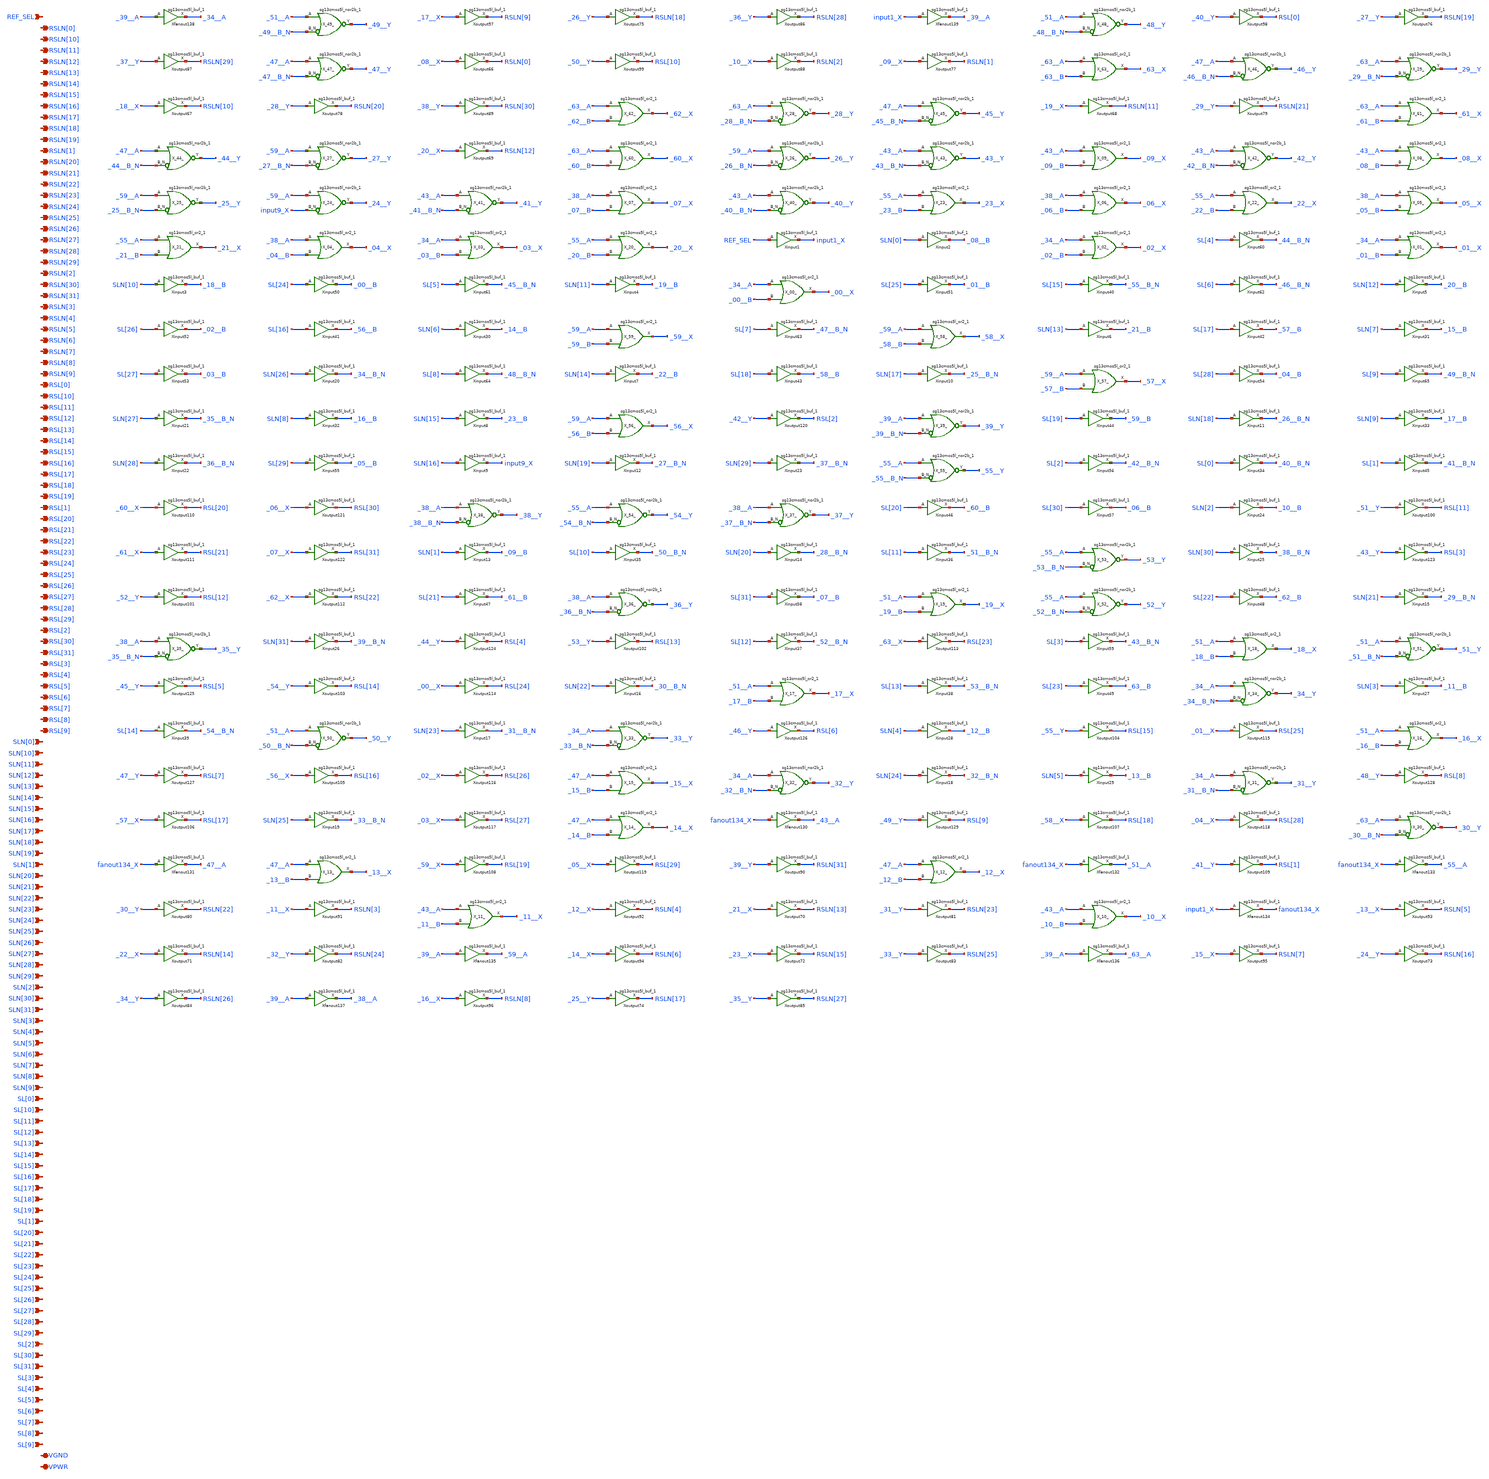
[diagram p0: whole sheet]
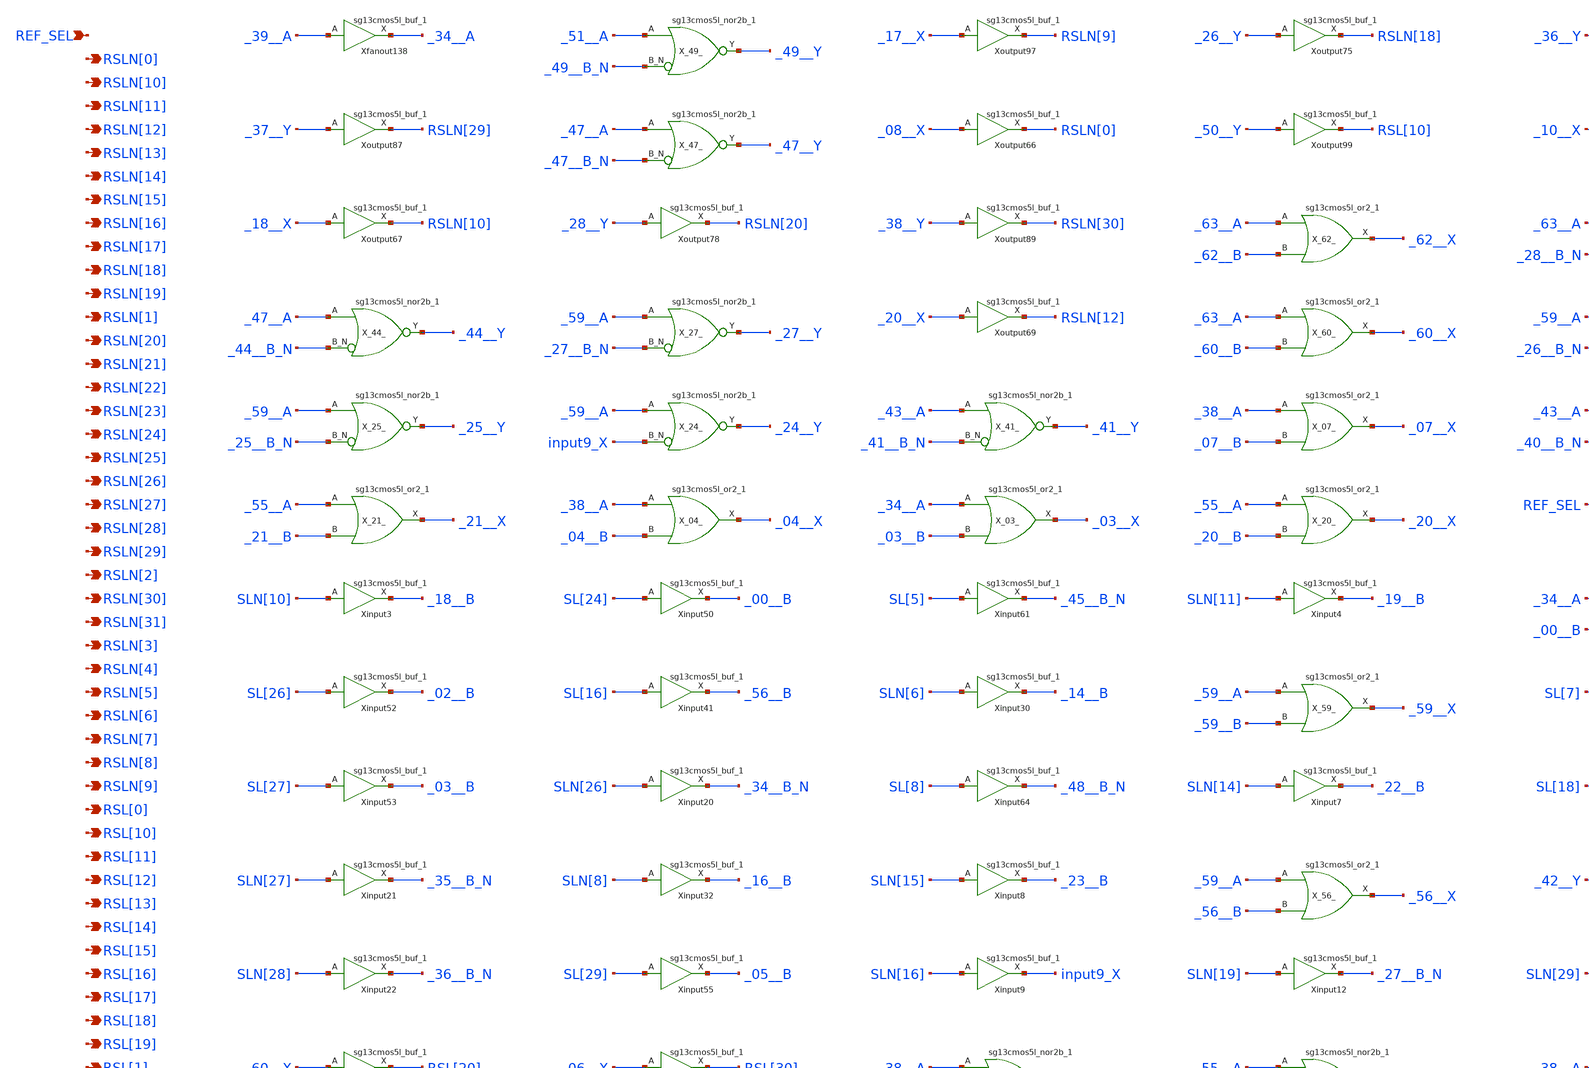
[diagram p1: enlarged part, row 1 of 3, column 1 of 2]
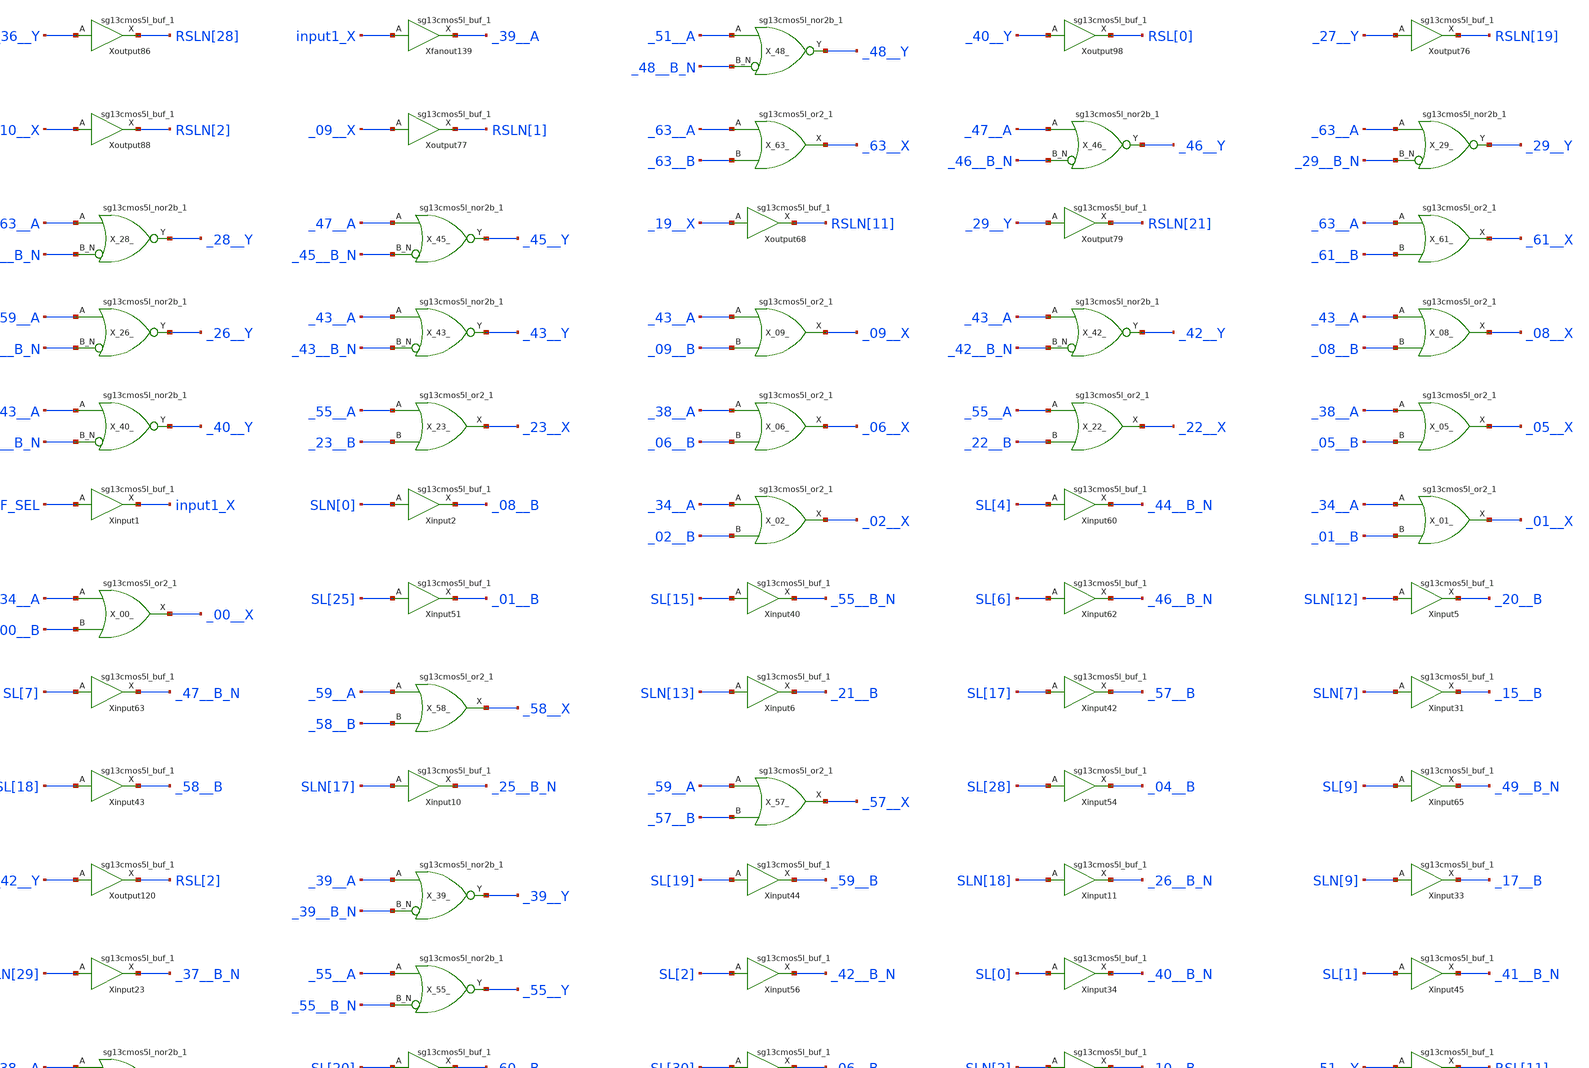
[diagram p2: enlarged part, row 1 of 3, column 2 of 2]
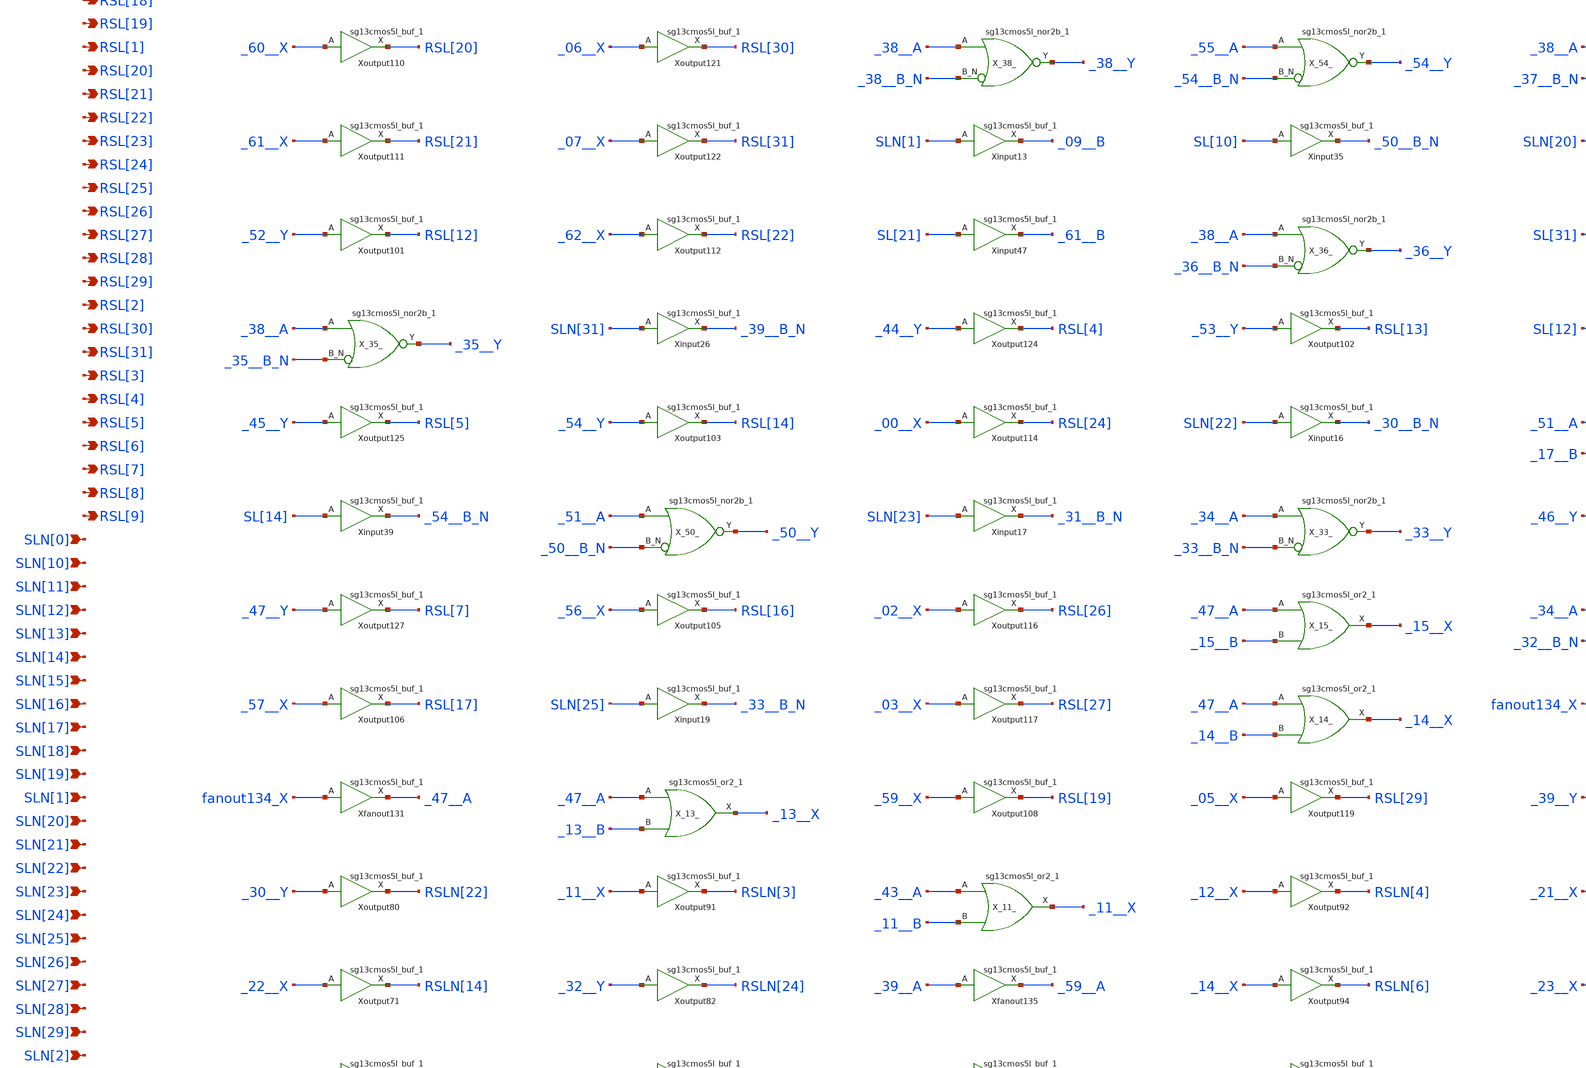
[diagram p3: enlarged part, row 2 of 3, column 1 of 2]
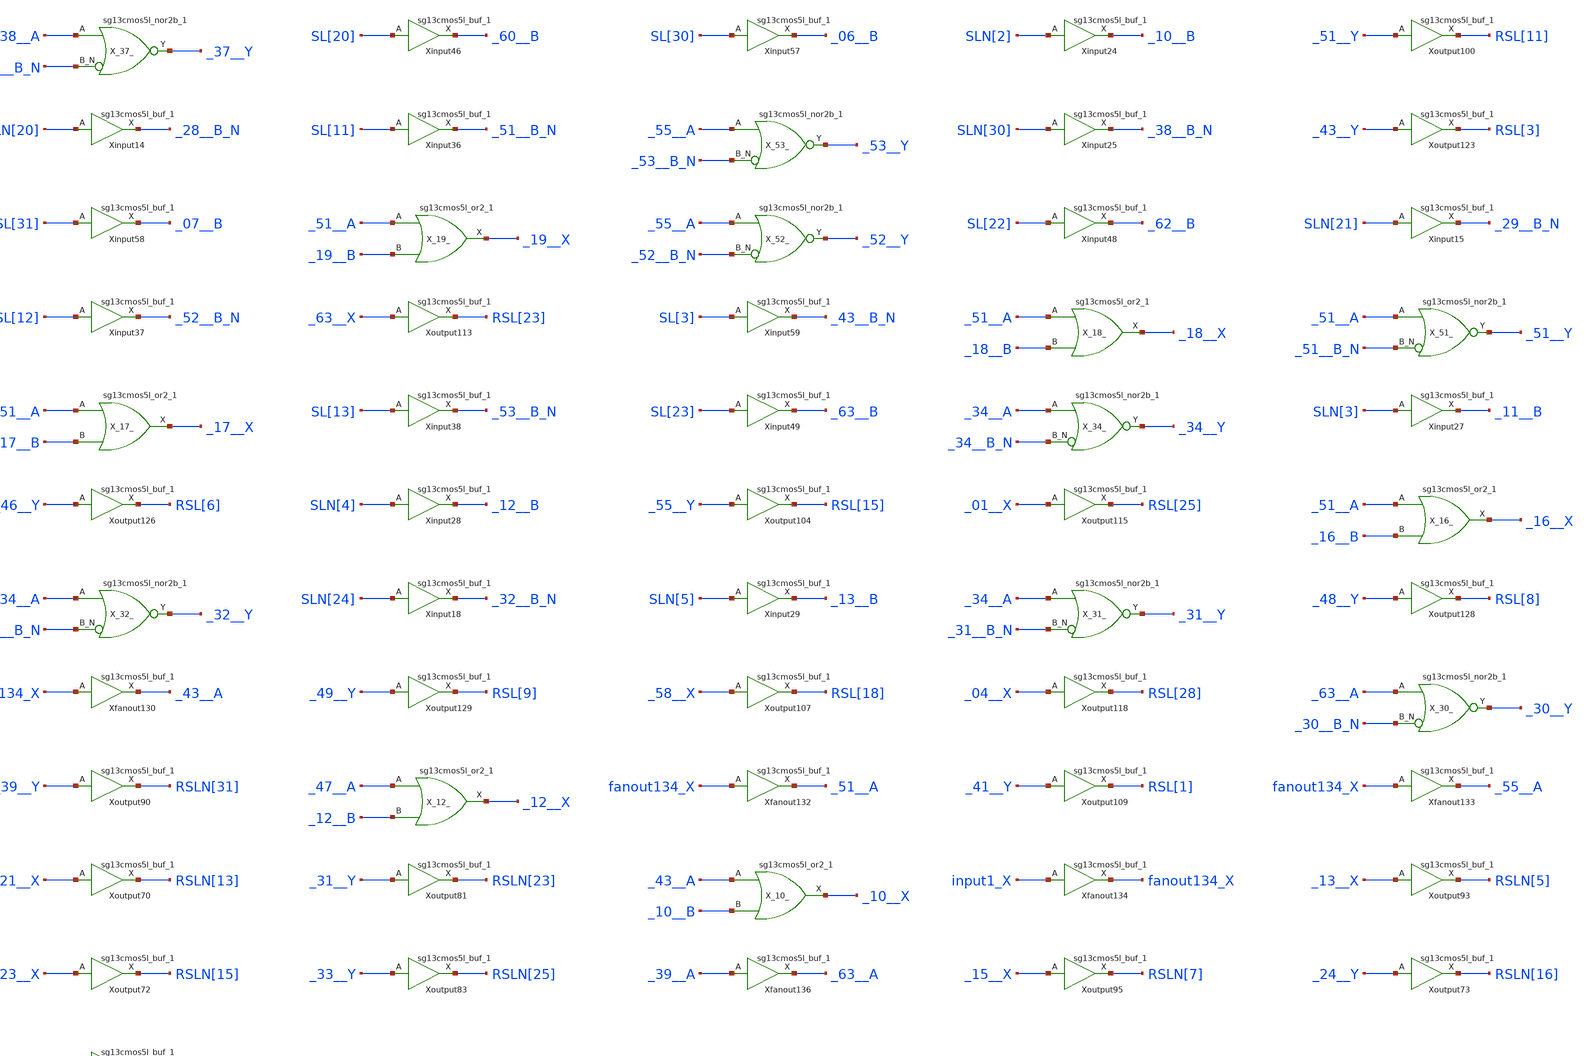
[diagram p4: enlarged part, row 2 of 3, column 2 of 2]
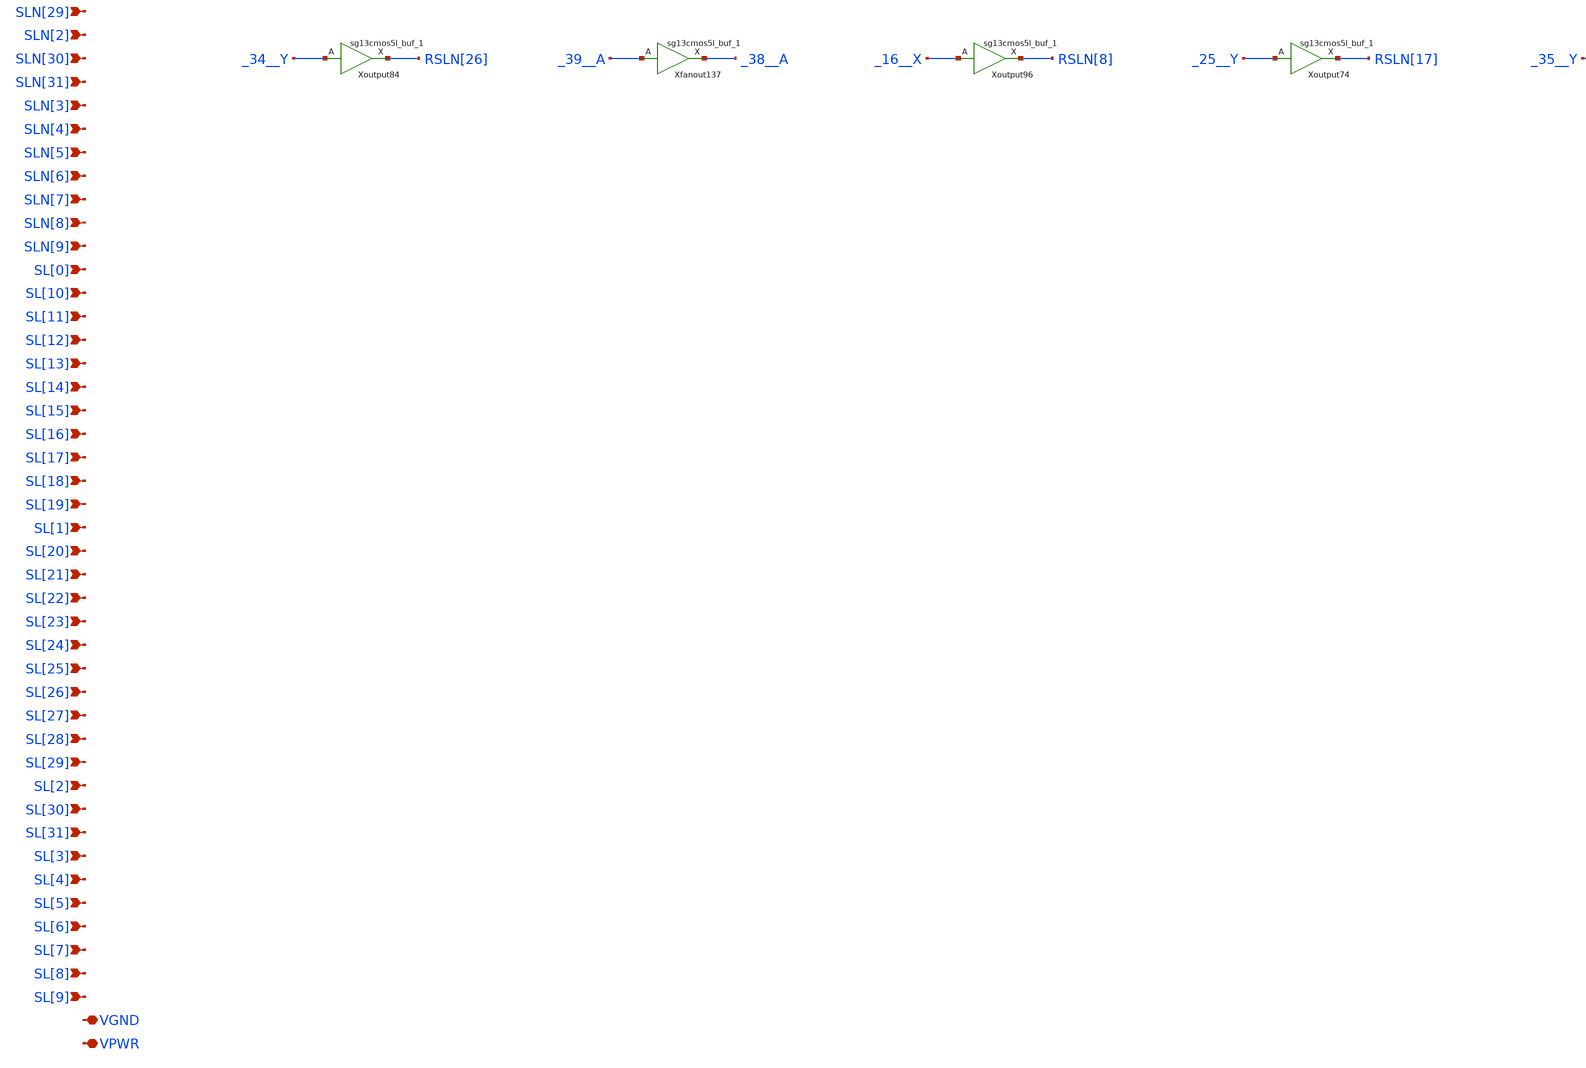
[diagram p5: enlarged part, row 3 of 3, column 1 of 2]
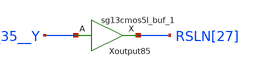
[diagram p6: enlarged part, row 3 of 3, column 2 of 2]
** sch_path: SoC6169-main/schematic/xschem/REFERENCE_MUX.sch
* Copyright 2026 USFQ CAM team
* Licensed under the Apache License, Version 2.0 (the "License");
* you may not use this file except in compliance with the License.
* You may obtain a copy of the License at
* https://www.apache.org/licenses/LICENSE-2.0
* Unless required by applicable law or agreed to in writing, software
* distributed under the License is distributed on an "AS IS" BASIS,
* WITHOUT WARRANTIES OR CONDITIONS OF ANY KIND, either express or implied.
* See the License for the specific language governing permissions and
* limitations under the License.
**.subckt REFERENCE_MUX REF_SEL RSLN[0] RSLN[10] RSLN[11] RSLN[12] RSLN[13] RSLN[14] RSLN[15]
*+ RSLN[16] RSLN[17] RSLN[18] RSLN[19] RSLN[1] RSLN[20] RSLN[21] RSLN[22] RSLN[23] RSLN[24] RSLN[25] RSLN[26]
*+ RSLN[27] RSLN[28] RSLN[29] RSLN[2] RSLN[30] RSLN[31] RSLN[3] RSLN[4] RSLN[5] RSLN[6] RSLN[7] RSLN[8] RSLN[9]
*+ RSL[0] RSL[10] RSL[11] RSL[12] RSL[13] RSL[14] RSL[15] RSL[16] RSL[17] RSL[18] RSL[19] RSL[1] RSL[20]
*+ RSL[21] RSL[22] RSL[23] RSL[24] RSL[25] RSL[26] RSL[27] RSL[28] RSL[29] RSL[2] RSL[30] RSL[31] RSL[3]
*+ RSL[4] RSL[5] RSL[6] RSL[7] RSL[8] RSL[9] SLN[0] SLN[10] SLN[11] SLN[12] SLN[13] SLN[14] SLN[15] SLN[16]
*+ SLN[17] SLN[18] SLN[19] SLN[1] SLN[20] SLN[21] SLN[22] SLN[23] SLN[24] SLN[25] SLN[26] SLN[27] SLN[28]
*+ SLN[29] SLN[2] SLN[30] SLN[31] SLN[3] SLN[4] SLN[5] SLN[6] SLN[7] SLN[8] SLN[9] SL[0] SL[10] SL[11] SL[12]
*+ SL[13] SL[14] SL[15] SL[16] SL[17] SL[18] SL[19] SL[1] SL[20] SL[21] SL[22] SL[23] SL[24] SL[25] SL[26]
*+ SL[27] SL[28] SL[29] SL[2] SL[30] SL[31] SL[3] SL[4] SL[5] SL[6] SL[7] SL[8] SL[9] VGND VPWR
*.ipin REF_SEL
*.opin RSLN[0]
*.opin RSLN[10]
*.opin RSLN[11]
*.opin RSLN[12]
*.opin RSLN[13]
*.opin RSLN[14]
*.opin RSLN[15]
*.opin RSLN[16]
*.opin RSLN[17]
*.opin RSLN[18]
*.opin RSLN[19]
*.opin RSLN[1]
*.opin RSLN[20]
*.opin RSLN[21]
*.opin RSLN[22]
*.opin RSLN[23]
*.opin RSLN[24]
*.opin RSLN[25]
*.opin RSLN[26]
*.opin RSLN[27]
*.opin RSLN[28]
*.opin RSLN[29]
*.opin RSLN[2]
*.opin RSLN[30]
*.opin RSLN[31]
*.opin RSLN[3]
*.opin RSLN[4]
*.opin RSLN[5]
*.opin RSLN[6]
*.opin RSLN[7]
*.opin RSLN[8]
*.opin RSLN[9]
*.opin RSL[0]
*.opin RSL[10]
*.opin RSL[11]
*.opin RSL[12]
*.opin RSL[13]
*.opin RSL[14]
*.opin RSL[15]
*.opin RSL[16]
*.opin RSL[17]
*.opin RSL[18]
*.opin RSL[19]
*.opin RSL[1]
*.opin RSL[20]
*.opin RSL[21]
*.opin RSL[22]
*.opin RSL[23]
*.opin RSL[24]
*.opin RSL[25]
*.opin RSL[26]
*.opin RSL[27]
*.opin RSL[28]
*.opin RSL[29]
*.opin RSL[2]
*.opin RSL[30]
*.opin RSL[31]
*.opin RSL[3]
*.opin RSL[4]
*.opin RSL[5]
*.opin RSL[6]
*.opin RSL[7]
*.opin RSL[8]
*.opin RSL[9]
*.ipin SLN[0]
*.ipin SLN[10]
*.ipin SLN[11]
*.ipin SLN[12]
*.ipin SLN[13]
*.ipin SLN[14]
*.ipin SLN[15]
*.ipin SLN[16]
*.ipin SLN[17]
*.ipin SLN[18]
*.ipin SLN[19]
*.ipin SLN[1]
*.ipin SLN[20]
*.ipin SLN[21]
*.ipin SLN[22]
*.ipin SLN[23]
*.ipin SLN[24]
*.ipin SLN[25]
*.ipin SLN[26]
*.ipin SLN[27]
*.ipin SLN[28]
*.ipin SLN[29]
*.ipin SLN[2]
*.ipin SLN[30]
*.ipin SLN[31]
*.ipin SLN[3]
*.ipin SLN[4]
*.ipin SLN[5]
*.ipin SLN[6]
*.ipin SLN[7]
*.ipin SLN[8]
*.ipin SLN[9]
*.ipin SL[0]
*.ipin SL[10]
*.ipin SL[11]
*.ipin SL[12]
*.ipin SL[13]
*.ipin SL[14]
*.ipin SL[15]
*.ipin SL[16]
*.ipin SL[17]
*.ipin SL[18]
*.ipin SL[19]
*.ipin SL[1]
*.ipin SL[20]
*.ipin SL[21]
*.ipin SL[22]
*.ipin SL[23]
*.ipin SL[24]
*.ipin SL[25]
*.ipin SL[26]
*.ipin SL[27]
*.ipin SL[28]
*.ipin SL[29]
*.ipin SL[2]
*.ipin SL[30]
*.ipin SL[31]
*.ipin SL[3]
*.ipin SL[4]
*.ipin SL[5]
*.ipin SL[6]
*.ipin SL[7]
*.ipin SL[8]
*.ipin SL[9]
*.iopin VGND
*.iopin VPWR
Xfanout138 _34__A _39__A VPWR VGND sg13cmos5l_buf_1
X_49_ _49__Y _51__A _49__B_N VPWR VGND sg13cmos5l_nor2b_1
Xoutput97 RSLN[9] _17__X VPWR VGND sg13cmos5l_buf_1
Xoutput75 RSLN[18] _26__Y VPWR VGND sg13cmos5l_buf_1
Xoutput86 RSLN[28] _36__Y VPWR VGND sg13cmos5l_buf_1
Xfanout139 _39__A input1_X VPWR VGND sg13cmos5l_buf_1
X_48_ _48__Y _51__A _48__B_N VPWR VGND sg13cmos5l_nor2b_1
Xoutput98 RSL[0] _40__Y VPWR VGND sg13cmos5l_buf_1
Xoutput76 RSLN[19] _27__Y VPWR VGND sg13cmos5l_buf_1
Xoutput87 RSLN[29] _37__Y VPWR VGND sg13cmos5l_buf_1
X_47_ _47__Y _47__A _47__B_N VPWR VGND sg13cmos5l_nor2b_1
Xoutput66 RSLN[0] _08__X VPWR VGND sg13cmos5l_buf_1
Xoutput99 RSL[10] _50__Y VPWR VGND sg13cmos5l_buf_1
Xoutput88 RSLN[2] _10__X VPWR VGND sg13cmos5l_buf_1
Xoutput77 RSLN[1] _09__X VPWR VGND sg13cmos5l_buf_1
X_63_ _63__X _63__A _63__B VPWR VGND sg13cmos5l_or2_1
X_46_ _46__Y _47__A _46__B_N VPWR VGND sg13cmos5l_nor2b_1
X_29_ _29__Y _63__A _29__B_N VPWR VGND sg13cmos5l_nor2b_1
Xoutput67 RSLN[10] _18__X VPWR VGND sg13cmos5l_buf_1
Xoutput78 RSLN[20] _28__Y VPWR VGND sg13cmos5l_buf_1
Xoutput89 RSLN[30] _38__Y VPWR VGND sg13cmos5l_buf_1
X_62_ _62__X _63__A _62__B VPWR VGND sg13cmos5l_or2_1
X_28_ _28__Y _63__A _28__B_N VPWR VGND sg13cmos5l_nor2b_1
X_45_ _45__Y _47__A _45__B_N VPWR VGND sg13cmos5l_nor2b_1
Xoutput68 RSLN[11] _19__X VPWR VGND sg13cmos5l_buf_1
Xoutput79 RSLN[21] _29__Y VPWR VGND sg13cmos5l_buf_1
X_61_ _61__X _63__A _61__B VPWR VGND sg13cmos5l_or2_1
X_44_ _44__Y _47__A _44__B_N VPWR VGND sg13cmos5l_nor2b_1
X_27_ _27__Y _59__A _27__B_N VPWR VGND sg13cmos5l_nor2b_1
Xoutput69 RSLN[12] _20__X VPWR VGND sg13cmos5l_buf_1
X_60_ _60__X _63__A _60__B VPWR VGND sg13cmos5l_or2_1
X_26_ _26__Y _59__A _26__B_N VPWR VGND sg13cmos5l_nor2b_1
X_43_ _43__Y _43__A _43__B_N VPWR VGND sg13cmos5l_nor2b_1
X_09_ _09__X _43__A _09__B VPWR VGND sg13cmos5l_or2_1
X_42_ _42__Y _43__A _42__B_N VPWR VGND sg13cmos5l_nor2b_1
X_08_ _08__X _43__A _08__B VPWR VGND sg13cmos5l_or2_1
X_25_ _25__Y _59__A _25__B_N VPWR VGND sg13cmos5l_nor2b_1
X_24_ _24__Y _59__A input9_X VPWR VGND sg13cmos5l_nor2b_1
X_41_ _41__Y _43__A _41__B_N VPWR VGND sg13cmos5l_nor2b_1
X_07_ _07__X _38__A _07__B VPWR VGND sg13cmos5l_or2_1
X_40_ _40__Y _43__A _40__B_N VPWR VGND sg13cmos5l_nor2b_1
X_23_ _23__X _55__A _23__B VPWR VGND sg13cmos5l_or2_1
X_06_ _06__X _38__A _06__B VPWR VGND sg13cmos5l_or2_1
X_22_ _22__X _55__A _22__B VPWR VGND sg13cmos5l_or2_1
X_05_ _05__X _38__A _05__B VPWR VGND sg13cmos5l_or2_1
X_21_ _21__X _55__A _21__B VPWR VGND sg13cmos5l_or2_1
X_04_ _04__X _38__A _04__B VPWR VGND sg13cmos5l_or2_1
X_03_ _03__X _34__A _03__B VPWR VGND sg13cmos5l_or2_1
X_20_ _20__X _55__A _20__B VPWR VGND sg13cmos5l_or2_1
Xinput1 input1_X REF_SEL VPWR VGND sg13cmos5l_buf_1
Xinput2 _08__B SLN[0] VPWR VGND sg13cmos5l_buf_1
X_02_ _02__X _34__A _02__B VPWR VGND sg13cmos5l_or2_1
Xinput60 _44__B_N SL[4] VPWR VGND sg13cmos5l_buf_1
X_01_ _01__X _34__A _01__B VPWR VGND sg13cmos5l_or2_1
Xinput3 _18__B SLN[10] VPWR VGND sg13cmos5l_buf_1
Xinput50 _00__B SL[24] VPWR VGND sg13cmos5l_buf_1
Xinput61 _45__B_N SL[5] VPWR VGND sg13cmos5l_buf_1
Xinput4 _19__B SLN[11] VPWR VGND sg13cmos5l_buf_1
X_00_ _00__X _34__A _00__B VPWR VGND sg13cmos5l_or2_1
Xinput51 _01__B SL[25] VPWR VGND sg13cmos5l_buf_1
Xinput40 _55__B_N SL[15] VPWR VGND sg13cmos5l_buf_1
Xinput62 _46__B_N SL[6] VPWR VGND sg13cmos5l_buf_1
Xinput5 _20__B SLN[12] VPWR VGND sg13cmos5l_buf_1
Xinput52 _02__B SL[26] VPWR VGND sg13cmos5l_buf_1
Xinput41 _56__B SL[16] VPWR VGND sg13cmos5l_buf_1
Xinput30 _14__B SLN[6] VPWR VGND sg13cmos5l_buf_1
X_59_ _59__X _59__A _59__B VPWR VGND sg13cmos5l_or2_1
Xinput63 _47__B_N SL[7] VPWR VGND sg13cmos5l_buf_1
X_58_ _58__X _59__A _58__B VPWR VGND sg13cmos5l_or2_1
Xinput6 _21__B SLN[13] VPWR VGND sg13cmos5l_buf_1
Xinput42 _57__B SL[17] VPWR VGND sg13cmos5l_buf_1
Xinput31 _15__B SLN[7] VPWR VGND sg13cmos5l_buf_1
Xinput53 _03__B SL[27] VPWR VGND sg13cmos5l_buf_1
Xinput20 _34__B_N SLN[26] VPWR VGND sg13cmos5l_buf_1
Xinput64 _48__B_N SL[8] VPWR VGND sg13cmos5l_buf_1
Xinput7 _22__B SLN[14] VPWR VGND sg13cmos5l_buf_1
Xinput43 _58__B SL[18] VPWR VGND sg13cmos5l_buf_1
Xinput10 _25__B_N SLN[17] VPWR VGND sg13cmos5l_buf_1
X_57_ _57__X _59__A _57__B VPWR VGND sg13cmos5l_or2_1
Xinput54 _04__B SL[28] VPWR VGND sg13cmos5l_buf_1
Xinput65 _49__B_N SL[9] VPWR VGND sg13cmos5l_buf_1
Xinput21 _35__B_N SLN[27] VPWR VGND sg13cmos5l_buf_1
Xinput32 _16__B SLN[8] VPWR VGND sg13cmos5l_buf_1
Xinput8 _23__B SLN[15] VPWR VGND sg13cmos5l_buf_1
X_56_ _56__X _59__A _56__B VPWR VGND sg13cmos5l_or2_1
Xoutput120 RSL[2] _42__Y VPWR VGND sg13cmos5l_buf_1
X_39_ _39__Y _39__A _39__B_N VPWR VGND sg13cmos5l_nor2b_1
Xinput44 _59__B SL[19] VPWR VGND sg13cmos5l_buf_1
Xinput11 _26__B_N SLN[18] VPWR VGND sg13cmos5l_buf_1
Xinput33 _17__B SLN[9] VPWR VGND sg13cmos5l_buf_1
Xinput22 _36__B_N SLN[28] VPWR VGND sg13cmos5l_buf_1
Xinput55 _05__B SL[29] VPWR VGND sg13cmos5l_buf_1
Xinput9 input9_X SLN[16] VPWR VGND sg13cmos5l_buf_1
Xinput12 _27__B_N SLN[19] VPWR VGND sg13cmos5l_buf_1
Xinput23 _37__B_N SLN[29] VPWR VGND sg13cmos5l_buf_1
X_55_ _55__Y _55__A _55__B_N VPWR VGND sg13cmos5l_nor2b_1
Xinput56 _42__B_N SL[2] VPWR VGND sg13cmos5l_buf_1
Xinput34 _40__B_N SL[0] VPWR VGND sg13cmos5l_buf_1
Xinput45 _41__B_N SL[1] VPWR VGND sg13cmos5l_buf_1
Xoutput110 RSL[20] _60__X VPWR VGND sg13cmos5l_buf_1
Xoutput121 RSL[30] _06__X VPWR VGND sg13cmos5l_buf_1
X_38_ _38__Y _38__A _38__B_N VPWR VGND sg13cmos5l_nor2b_1
X_54_ _54__Y _55__A _54__B_N VPWR VGND sg13cmos5l_nor2b_1
X_37_ _37__Y _38__A _37__B_N VPWR VGND sg13cmos5l_nor2b_1
Xinput46 _60__B SL[20] VPWR VGND sg13cmos5l_buf_1
Xinput57 _06__B SL[30] VPWR VGND sg13cmos5l_buf_1
Xinput24 _10__B SLN[2] VPWR VGND sg13cmos5l_buf_1
Xoutput100 RSL[11] _51__Y VPWR VGND sg13cmos5l_buf_1
Xoutput111 RSL[21] _61__X VPWR VGND sg13cmos5l_buf_1
Xoutput122 RSL[31] _07__X VPWR VGND sg13cmos5l_buf_1
Xinput13 _09__B SLN[1] VPWR VGND sg13cmos5l_buf_1
Xinput35 _50__B_N SL[10] VPWR VGND sg13cmos5l_buf_1
Xinput14 _28__B_N SLN[20] VPWR VGND sg13cmos5l_buf_1
Xinput36 _51__B_N SL[11] VPWR VGND sg13cmos5l_buf_1
X_53_ _53__Y _55__A _53__B_N VPWR VGND sg13cmos5l_nor2b_1
Xinput25 _38__B_N SLN[30] VPWR VGND sg13cmos5l_buf_1
Xoutput123 RSL[3] _43__Y VPWR VGND sg13cmos5l_buf_1
Xoutput101 RSL[12] _52__Y VPWR VGND sg13cmos5l_buf_1
Xoutput112 RSL[22] _62__X VPWR VGND sg13cmos5l_buf_1
Xinput47 _61__B SL[21] VPWR VGND sg13cmos5l_buf_1
X_36_ _36__Y _38__A _36__B_N VPWR VGND sg13cmos5l_nor2b_1
Xinput58 _07__B SL[31] VPWR VGND sg13cmos5l_buf_1
X_19_ _19__X _51__A _19__B VPWR VGND sg13cmos5l_or2_1
X_52_ _52__Y _55__A _52__B_N VPWR VGND sg13cmos5l_nor2b_1
Xinput48 _62__B SL[22] VPWR VGND sg13cmos5l_buf_1
Xinput15 _29__B_N SLN[21] VPWR VGND sg13cmos5l_buf_1
X_35_ _35__Y _38__A _35__B_N VPWR VGND sg13cmos5l_nor2b_1
Xinput26 _39__B_N SLN[31] VPWR VGND sg13cmos5l_buf_1
Xoutput124 RSL[4] _44__Y VPWR VGND sg13cmos5l_buf_1
Xoutput102 RSL[13] _53__Y VPWR VGND sg13cmos5l_buf_1
Xinput37 _52__B_N SL[12] VPWR VGND sg13cmos5l_buf_1
Xoutput113 RSL[23] _63__X VPWR VGND sg13cmos5l_buf_1
Xinput59 _43__B_N SL[3] VPWR VGND sg13cmos5l_buf_1
X_18_ _18__X _51__A _18__B VPWR VGND sg13cmos5l_or2_1
X_51_ _51__Y _51__A _51__B_N VPWR VGND sg13cmos5l_nor2b_1
Xoutput125 RSL[5] _45__Y VPWR VGND sg13cmos5l_buf_1
Xoutput103 RSL[14] _54__Y VPWR VGND sg13cmos5l_buf_1
Xoutput114 RSL[24] _00__X VPWR VGND sg13cmos5l_buf_1
Xinput16 _30__B_N SLN[22] VPWR VGND sg13cmos5l_buf_1
X_17_ _17__X _51__A _17__B VPWR VGND sg13cmos5l_or2_1
Xinput38 _53__B_N SL[13] VPWR VGND sg13cmos5l_buf_1
Xinput49 _63__B SL[23] VPWR VGND sg13cmos5l_buf_1
X_34_ _34__Y _34__A _34__B_N VPWR VGND sg13cmos5l_nor2b_1
Xinput27 _11__B SLN[3] VPWR VGND sg13cmos5l_buf_1
Xinput39 _54__B_N SL[14] VPWR VGND sg13cmos5l_buf_1
X_50_ _50__Y _51__A _50__B_N VPWR VGND sg13cmos5l_nor2b_1
Xinput17 _31__B_N SLN[23] VPWR VGND sg13cmos5l_buf_1
X_33_ _33__Y _34__A _33__B_N VPWR VGND sg13cmos5l_nor2b_1
Xoutput126 RSL[6] _46__Y VPWR VGND sg13cmos5l_buf_1
Xinput28 _12__B SLN[4] VPWR VGND sg13cmos5l_buf_1
Xoutput104 RSL[15] _55__Y VPWR VGND sg13cmos5l_buf_1
Xoutput115 RSL[25] _01__X VPWR VGND sg13cmos5l_buf_1
X_16_ _16__X _51__A _16__B VPWR VGND sg13cmos5l_or2_1
Xoutput127 RSL[7] _47__Y VPWR VGND sg13cmos5l_buf_1
Xoutput105 RSL[16] _56__X VPWR VGND sg13cmos5l_buf_1
Xoutput116 RSL[26] _02__X VPWR VGND sg13cmos5l_buf_1
X_15_ _15__X _47__A _15__B VPWR VGND sg13cmos5l_or2_1
X_32_ _32__Y _34__A _32__B_N VPWR VGND sg13cmos5l_nor2b_1
Xinput18 _32__B_N SLN[24] VPWR VGND sg13cmos5l_buf_1
Xinput29 _13__B SLN[5] VPWR VGND sg13cmos5l_buf_1
X_31_ _31__Y _34__A _31__B_N VPWR VGND sg13cmos5l_nor2b_1
Xoutput128 RSL[8] _48__Y VPWR VGND sg13cmos5l_buf_1
Xoutput106 RSL[17] _57__X VPWR VGND sg13cmos5l_buf_1
Xinput19 _33__B_N SLN[25] VPWR VGND sg13cmos5l_buf_1
Xoutput117 RSL[27] _03__X VPWR VGND sg13cmos5l_buf_1
X_14_ _14__X _47__A _14__B VPWR VGND sg13cmos5l_or2_1
Xfanout130 _43__A fanout134_X VPWR VGND sg13cmos5l_buf_1
Xoutput129 RSL[9] _49__Y VPWR VGND sg13cmos5l_buf_1
Xoutput107 RSL[18] _58__X VPWR VGND sg13cmos5l_buf_1
Xoutput118 RSL[28] _04__X VPWR VGND sg13cmos5l_buf_1
X_30_ _30__Y _63__A _30__B_N VPWR VGND sg13cmos5l_nor2b_1
Xfanout131 _47__A fanout134_X VPWR VGND sg13cmos5l_buf_1
X_13_ _13__X _47__A _13__B VPWR VGND sg13cmos5l_or2_1
Xoutput108 RSL[19] _59__X VPWR VGND sg13cmos5l_buf_1
Xoutput119 RSL[29] _05__X VPWR VGND sg13cmos5l_buf_1
Xoutput90 RSLN[31] _39__Y VPWR VGND sg13cmos5l_buf_1
X_12_ _12__X _47__A _12__B VPWR VGND sg13cmos5l_or2_1
Xfanout132 _51__A fanout134_X VPWR VGND sg13cmos5l_buf_1
Xoutput109 RSL[1] _41__Y VPWR VGND sg13cmos5l_buf_1
Xfanout133 _55__A fanout134_X VPWR VGND sg13cmos5l_buf_1
Xoutput80 RSLN[22] _30__Y VPWR VGND sg13cmos5l_buf_1
Xoutput91 RSLN[3] _11__X VPWR VGND sg13cmos5l_buf_1
X_11_ _11__X _43__A _11__B VPWR VGND sg13cmos5l_or2_1
Xoutput92 RSLN[4] _12__X VPWR VGND sg13cmos5l_buf_1
Xoutput70 RSLN[13] _21__X VPWR VGND sg13cmos5l_buf_1
Xoutput81 RSLN[23] _31__Y VPWR VGND sg13cmos5l_buf_1
X_10_ _10__X _43__A _10__B VPWR VGND sg13cmos5l_or2_1
Xfanout134 fanout134_X input1_X VPWR VGND sg13cmos5l_buf_1
Xoutput93 RSLN[5] _13__X VPWR VGND sg13cmos5l_buf_1
Xoutput71 RSLN[14] _22__X VPWR VGND sg13cmos5l_buf_1
Xoutput82 RSLN[24] _32__Y VPWR VGND sg13cmos5l_buf_1
Xfanout135 _59__A _39__A VPWR VGND sg13cmos5l_buf_1
Xoutput94 RSLN[6] _14__X VPWR VGND sg13cmos5l_buf_1
Xoutput72 RSLN[15] _23__X VPWR VGND sg13cmos5l_buf_1
Xoutput83 RSLN[25] _33__Y VPWR VGND sg13cmos5l_buf_1
Xfanout136 _63__A _39__A VPWR VGND sg13cmos5l_buf_1
Xoutput95 RSLN[7] _15__X VPWR VGND sg13cmos5l_buf_1
Xoutput73 RSLN[16] _24__Y VPWR VGND sg13cmos5l_buf_1
Xoutput84 RSLN[26] _34__Y VPWR VGND sg13cmos5l_buf_1
Xfanout137 _38__A _39__A VPWR VGND sg13cmos5l_buf_1
Xoutput96 RSLN[8] _16__X VPWR VGND sg13cmos5l_buf_1
Xoutput74 RSLN[17] _25__Y VPWR VGND sg13cmos5l_buf_1
Xoutput85 RSLN[27] _35__Y VPWR VGND sg13cmos5l_buf_1
**.ends
.end
